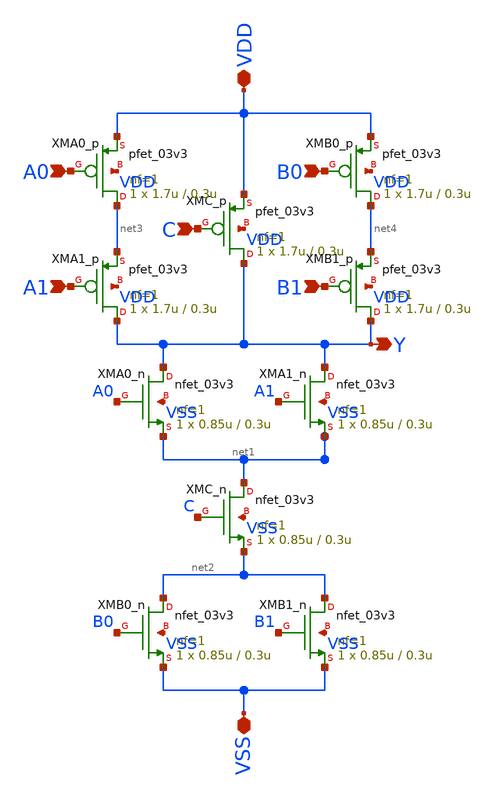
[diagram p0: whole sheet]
** sch_path: designs/oai221/gf180mcu_gp9t3v3_oai221_1.sch
**.subckt gf180mcu_gp9t3v3_oai221_1 A0 A1 C B0 B1 Y VSS VDD
*.ipin A0
*.ipin A1
*.ipin C
*.ipin B0
*.ipin B1
*.opin Y
*.iopin VSS
*.iopin VDD
XMB0_n net2 B0 VSS VSS nfet_03v3 L=0.3u W=0.85u nf=1 ad='int((nf+1)/2) * W/nf * 0.18u' as='int((nf+2)/2) * W/nf * 0.18u'
+ pd='2*int((nf+1)/2) * (W/nf + 0.18u)' ps='2*int((nf+2)/2) * (W/nf + 0.18u)' nrd='0.18u / W' nrs='0.18u / W'
+ sa=0 sb=0 sd=0 m=1
XMC_p Y C VDD VDD pfet_03v3 L=0.3u W=1.7u nf=1 ad='int((nf+1)/2) * W/nf * 0.18u' as='int((nf+2)/2) * W/nf * 0.18u'
+ pd='2*int((nf+1)/2) * (W/nf + 0.18u)' ps='2*int((nf+2)/2) * (W/nf + 0.18u)' nrd='0.18u / W' nrs='0.18u / W'
+ sa=0 sb=0 sd=0 m=1
XMB1_n net2 B1 VSS VSS nfet_03v3 L=0.3u W=0.85u nf=1 ad='int((nf+1)/2) * W/nf * 0.18u' as='int((nf+2)/2) * W/nf * 0.18u'
+ pd='2*int((nf+1)/2) * (W/nf + 0.18u)' ps='2*int((nf+2)/2) * (W/nf + 0.18u)' nrd='0.18u / W' nrs='0.18u / W'
+ sa=0 sb=0 sd=0 m=1
XMC_n net1 C net2 VSS nfet_03v3 L=0.3u W=0.85u nf=1 ad='int((nf+1)/2) * W/nf * 0.18u' as='int((nf+2)/2) * W/nf * 0.18u'
+ pd='2*int((nf+1)/2) * (W/nf + 0.18u)' ps='2*int((nf+2)/2) * (W/nf + 0.18u)' nrd='0.18u / W' nrs='0.18u / W'
+ sa=0 sb=0 sd=0 m=1
XMA0_n Y A0 net1 VSS nfet_03v3 L=0.3u W=0.85u nf=1 ad='int((nf+1)/2) * W/nf * 0.18u' as='int((nf+2)/2) * W/nf * 0.18u'
+ pd='2*int((nf+1)/2) * (W/nf + 0.18u)' ps='2*int((nf+2)/2) * (W/nf + 0.18u)' nrd='0.18u / W' nrs='0.18u / W'
+ sa=0 sb=0 sd=0 m=1
XMA1_n Y A1 net1 VSS nfet_03v3 L=0.3u W=0.85u nf=1 ad='int((nf+1)/2) * W/nf * 0.18u' as='int((nf+2)/2) * W/nf * 0.18u'
+ pd='2*int((nf+1)/2) * (W/nf + 0.18u)' ps='2*int((nf+2)/2) * (W/nf + 0.18u)' nrd='0.18u / W' nrs='0.18u / W'
+ sa=0 sb=0 sd=0 m=1
XMA1_p Y A1 net3 VDD pfet_03v3 L=0.3u W=1.7u nf=1 ad='int((nf+1)/2) * W/nf * 0.18u' as='int((nf+2)/2) * W/nf * 0.18u'
+ pd='2*int((nf+1)/2) * (W/nf + 0.18u)' ps='2*int((nf+2)/2) * (W/nf + 0.18u)' nrd='0.18u / W' nrs='0.18u / W'
+ sa=0 sb=0 sd=0 m=1
XMB1_p Y B1 net4 VDD pfet_03v3 L=0.3u W=1.7u nf=1 ad='int((nf+1)/2) * W/nf * 0.18u' as='int((nf+2)/2) * W/nf * 0.18u'
+ pd='2*int((nf+1)/2) * (W/nf + 0.18u)' ps='2*int((nf+2)/2) * (W/nf + 0.18u)' nrd='0.18u / W' nrs='0.18u / W'
+ sa=0 sb=0 sd=0 m=1
XMA0_p net3 A0 VDD VDD pfet_03v3 L=0.3u W=1.7u nf=1 ad='int((nf+1)/2) * W/nf * 0.18u' as='int((nf+2)/2) * W/nf * 0.18u'
+ pd='2*int((nf+1)/2) * (W/nf + 0.18u)' ps='2*int((nf+2)/2) * (W/nf + 0.18u)' nrd='0.18u / W' nrs='0.18u / W'
+ sa=0 sb=0 sd=0 m=1
XMB0_p net4 B0 VDD VDD pfet_03v3 L=0.3u W=1.7u nf=1 ad='int((nf+1)/2) * W/nf * 0.18u' as='int((nf+2)/2) * W/nf * 0.18u'
+ pd='2*int((nf+1)/2) * (W/nf + 0.18u)' ps='2*int((nf+2)/2) * (W/nf + 0.18u)' nrd='0.18u / W' nrs='0.18u / W'
+ sa=0 sb=0 sd=0 m=1
**.ends
.end
